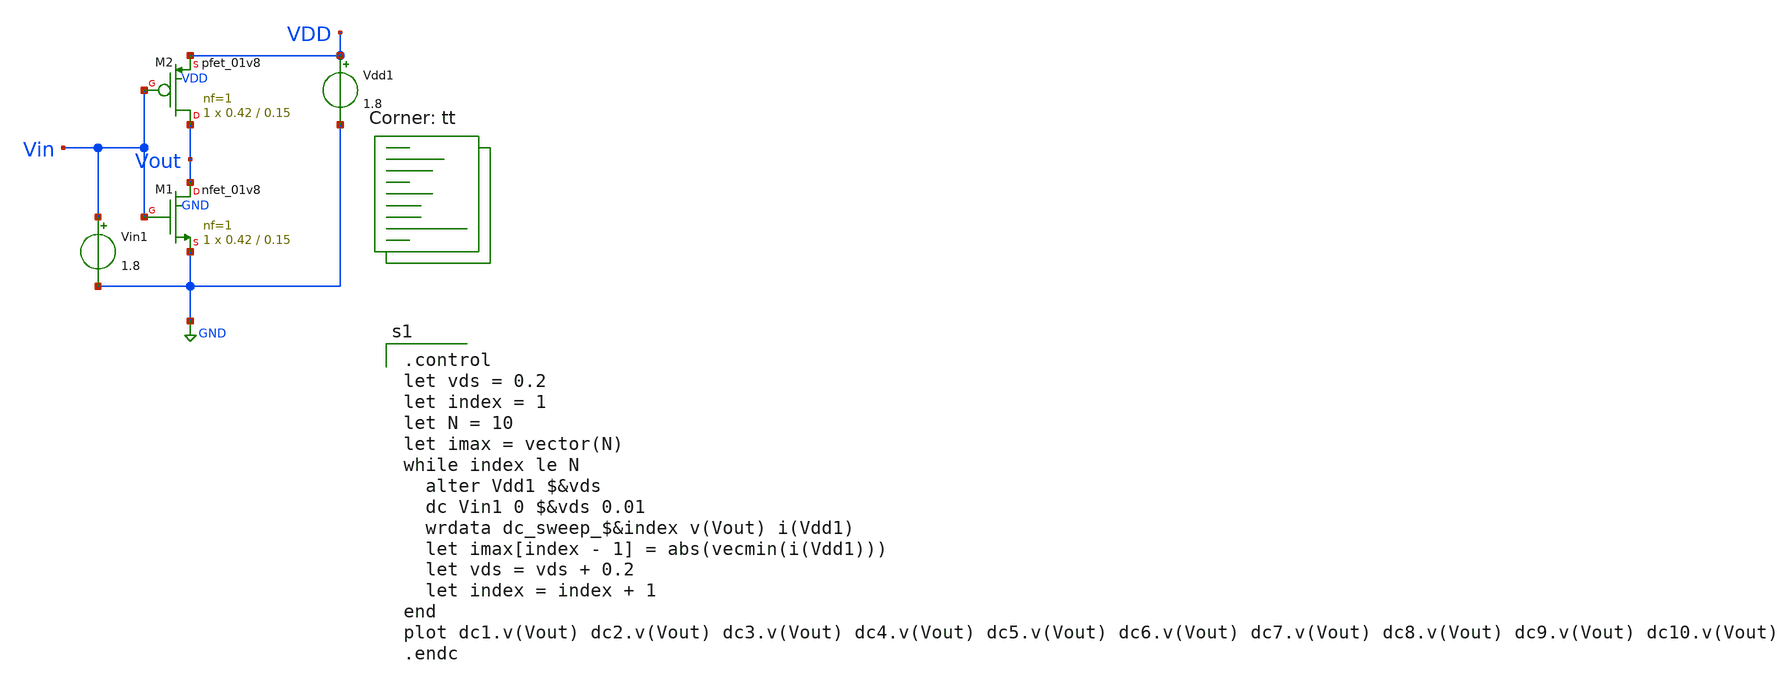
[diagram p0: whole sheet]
** sch_path: tut2/expt2_1/expt2_1.sch
**.subckt expt2_1
XM1 Vout Vin GND GND sky130_fd_pr__nfet_01v8 L=0.15 W=0.42 nf=1 ad='int((nf+1)/2) * W/nf * 0.29' as='int((nf+2)/2) * W/nf * 0.29'
+ pd='2*int((nf+1)/2) * (W/nf + 0.29)' ps='2*int((nf+2)/2) * (W/nf + 0.29)' nrd='0.29 / W' nrs='0.29 / W'
+ sa=0 sb=0 sd=0 mult=1 m=1
Vin1 Vin GND 1.8
XM2 Vout Vin VDD VDD sky130_fd_pr__pfet_01v8 L=0.15 W=0.42 nf=1 ad='int((nf+1)/2) * W/nf * 0.29' as='int((nf+2)/2) * W/nf * 0.29'
+ pd='2*int((nf+1)/2) * (W/nf + 0.29)' ps='2*int((nf+2)/2) * (W/nf + 0.29)' nrd='0.29 / W' nrs='0.29 / W'
+ sa=0 sb=0 sd=0 mult=1 m=1
Vdd1 VDD GND 1.8
**** begin user architecture code
.lib $::SKYWATER_MODELS/sky130.lib.spice tt

.control
let vds = 0.2
let index = 1
let N = 10
let imax = vector(N)
while index le N
  alter Vdd1 $&vds
  dc Vin1 0 $&vds 0.01
  wrdata dc_sweep_$&index v(Vout) i(Vdd1)
  let imax[index - 1] = abs(vecmin(i(Vdd1)))
  let vds = vds + 0.2
  let index = index + 1
end
plot dc1.v(Vout) dc2.v(Vout) dc3.v(Vout) dc4.v(Vout) dc5.v(Vout) dc6.v(Vout) dc7.v(Vout) dc8.v(Vout)
+ dc9.v(Vout) dc10.v(Vout)
.endc

**** end user architecture code
**.ends
.GLOBAL GND
.end
